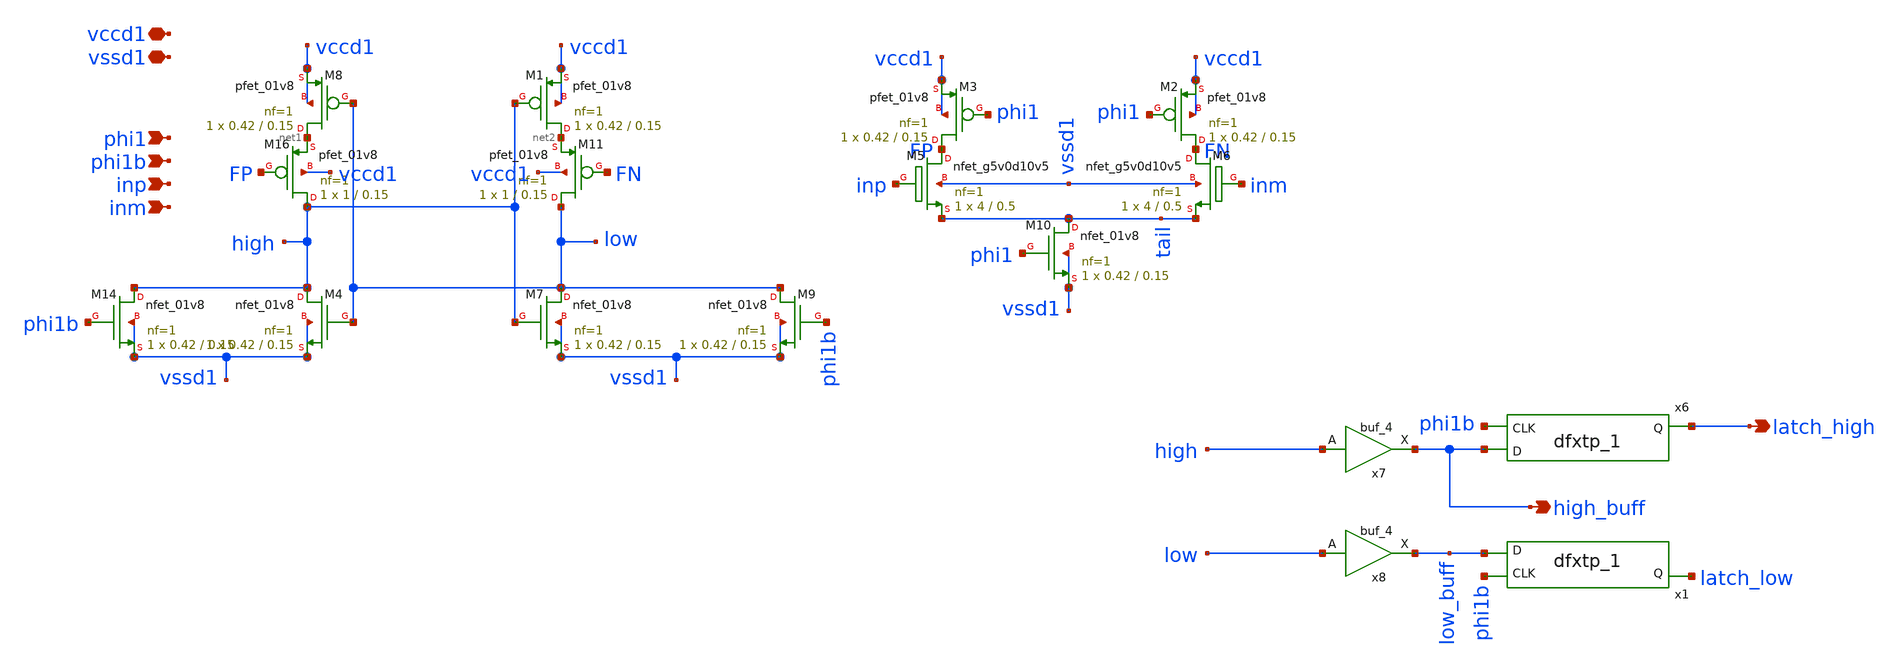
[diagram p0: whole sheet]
** sch_path: xschem/comparator.sch
**.subckt comparator phi1 phi1b inp inm vccd1 vssd1 latch_high high_buff
*.ipin phi1
*.ipin phi1b
*.ipin inp
*.ipin inm
*.iopin vccd1
*.iopin vssd1
*.opin latch_high
*.opin high_buff
XM16 high FP net1 vccd1 sky130_fd_pr__pfet_01v8 L=0.15 W=1 nf=1 ad='int((nf+1)/2) * W/nf * 0.29' as='int((nf+2)/2) * W/nf * 0.29'
+ pd='2*int((nf+1)/2) * (W/nf + 0.29)' ps='2*int((nf+2)/2) * (W/nf + 0.29)' nrd='0.29 / W' nrs='0.29 / W'
+ sa=0 sb=0 sd=0 mult=1 m=1
XM11 low FN net2 vccd1 sky130_fd_pr__pfet_01v8 L=0.15 W=1 nf=1 ad='int((nf+1)/2) * W/nf * 0.29' as='int((nf+2)/2) * W/nf * 0.29'
+ pd='2*int((nf+1)/2) * (W/nf + 0.29)' ps='2*int((nf+2)/2) * (W/nf + 0.29)' nrd='0.29 / W' nrs='0.29 / W'
+ sa=0 sb=0 sd=0 mult=1 m=1
XM5 FP inp tail vssd1 sky130_fd_pr__nfet_g5v0d10v5 L=0.5 W=4 nf=1 ad='int((nf+1)/2) * W/nf * 0.29' as='int((nf+2)/2) * W/nf * 0.29'
+ pd='2*int((nf+1)/2) * (W/nf + 0.29)' ps='2*int((nf+2)/2) * (W/nf + 0.29)' nrd='0.29 / W' nrs='0.29 / W'
+ sa=0 sb=0 sd=0 mult=1 m=1
XM6 FN inm tail vssd1 sky130_fd_pr__nfet_g5v0d10v5 L=0.5 W=4 nf=1 ad='int((nf+1)/2) * W/nf * 0.29' as='int((nf+2)/2) * W/nf * 0.29'
+ pd='2*int((nf+1)/2) * (W/nf + 0.29)' ps='2*int((nf+2)/2) * (W/nf + 0.29)' nrd='0.29 / W' nrs='0.29 / W'
+ sa=0 sb=0 sd=0 mult=1 m=1
XM8 net1 low vccd1 vccd1 sky130_fd_pr__pfet_01v8 L=0.15 W=0.42 nf=1 ad='int((nf+1)/2) * W/nf * 0.29'
+ as='int((nf+2)/2) * W/nf * 0.29' pd='2*int((nf+1)/2) * (W/nf + 0.29)' ps='2*int((nf+2)/2) * (W/nf + 0.29)'
+ nrd='0.29 / W' nrs='0.29 / W' sa=0 sb=0 sd=0 mult=1 m=1
XM1 net2 high vccd1 vccd1 sky130_fd_pr__pfet_01v8 L=0.15 W=0.42 nf=1 ad='int((nf+1)/2) * W/nf * 0.29'
+ as='int((nf+2)/2) * W/nf * 0.29' pd='2*int((nf+1)/2) * (W/nf + 0.29)' ps='2*int((nf+2)/2) * (W/nf + 0.29)'
+ nrd='0.29 / W' nrs='0.29 / W' sa=0 sb=0 sd=0 mult=1 m=1
XM14 high phi1b vssd1 vssd1 sky130_fd_pr__nfet_01v8 L=0.15 W=0.42 nf=1 ad='int((nf+1)/2) * W/nf * 0.29'
+ as='int((nf+2)/2) * W/nf * 0.29' pd='2*int((nf+1)/2) * (W/nf + 0.29)' ps='2*int((nf+2)/2) * (W/nf + 0.29)'
+ nrd='0.29 / W' nrs='0.29 / W' sa=0 sb=0 sd=0 mult=1 m=1
XM4 high low vssd1 vssd1 sky130_fd_pr__nfet_01v8 L=0.15 W=0.42 nf=1 ad='int((nf+1)/2) * W/nf * 0.29'
+ as='int((nf+2)/2) * W/nf * 0.29' pd='2*int((nf+1)/2) * (W/nf + 0.29)' ps='2*int((nf+2)/2) * (W/nf + 0.29)'
+ nrd='0.29 / W' nrs='0.29 / W' sa=0 sb=0 sd=0 mult=1 m=1
XM7 low high vssd1 vssd1 sky130_fd_pr__nfet_01v8 L=0.15 W=0.42 nf=1 ad='int((nf+1)/2) * W/nf * 0.29'
+ as='int((nf+2)/2) * W/nf * 0.29' pd='2*int((nf+1)/2) * (W/nf + 0.29)' ps='2*int((nf+2)/2) * (W/nf + 0.29)'
+ nrd='0.29 / W' nrs='0.29 / W' sa=0 sb=0 sd=0 mult=1 m=1
XM9 low phi1b vssd1 vssd1 sky130_fd_pr__nfet_01v8 L=0.15 W=0.42 nf=1 ad='int((nf+1)/2) * W/nf * 0.29'
+ as='int((nf+2)/2) * W/nf * 0.29' pd='2*int((nf+1)/2) * (W/nf + 0.29)' ps='2*int((nf+2)/2) * (W/nf + 0.29)'
+ nrd='0.29 / W' nrs='0.29 / W' sa=0 sb=0 sd=0 mult=1 m=1
XM2 FN phi1 vccd1 vccd1 sky130_fd_pr__pfet_01v8 L=0.15 W=0.42 nf=1 ad='int((nf+1)/2) * W/nf * 0.29' as='int((nf+2)/2) * W/nf * 0.29'
+ pd='2*int((nf+1)/2) * (W/nf + 0.29)' ps='2*int((nf+2)/2) * (W/nf + 0.29)' nrd='0.29 / W' nrs='0.29 / W'
+ sa=0 sb=0 sd=0 mult=1 m=1
XM3 FP phi1 vccd1 vccd1 sky130_fd_pr__pfet_01v8 L=0.15 W=0.42 nf=1 ad='int((nf+1)/2) * W/nf * 0.29' as='int((nf+2)/2) * W/nf * 0.29'
+ pd='2*int((nf+1)/2) * (W/nf + 0.29)' ps='2*int((nf+2)/2) * (W/nf + 0.29)' nrd='0.29 / W' nrs='0.29 / W'
+ sa=0 sb=0 sd=0 mult=1 m=1
XM10 tail phi1 vssd1 vssd1 sky130_fd_pr__nfet_01v8 L=0.15 W=0.42 nf=1 ad='int((nf+1)/2) * W/nf * 0.29'
+ as='int((nf+2)/2) * W/nf * 0.29' pd='2*int((nf+1)/2) * (W/nf + 0.29)' ps='2*int((nf+2)/2) * (W/nf + 0.29)'
+ nrd='0.29 / W' nrs='0.29 / W' sa=0 sb=0 sd=0 mult=1 m=1
x6 phi1b high_buff vssd1 vssd1 vccd1 vccd1 latch_high sky130_fd_sc_hd__dfxtp_1
x7 high vssd1 vssd1 vccd1 vccd1 high_buff sky130_fd_sc_hd__buf_4
x8 low vssd1 vssd1 vccd1 vccd1 low_buff sky130_fd_sc_hd__buf_4
x1 phi1b low_buff vssd1 vssd1 vccd1 vccd1 latch_low sky130_fd_sc_hd__dfxtp_1
**** begin user architecture code
 .lib $::SKYWATER_MODELS/sky130.lib.spice tt
.include $::SKYWATER_STDCELLS/sky130_fd_sc_hd.spice

**** end user architecture code
**.ends
.end
